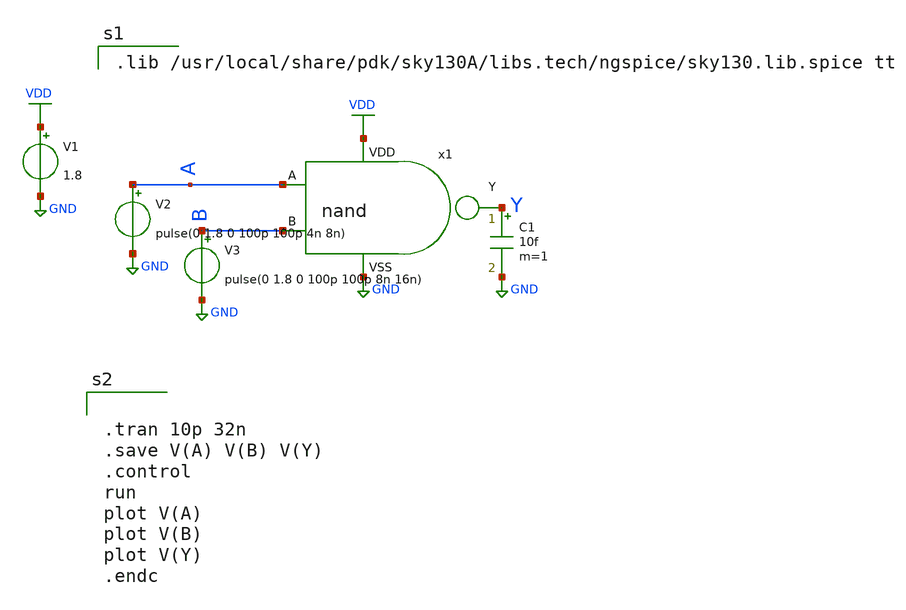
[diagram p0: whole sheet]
** sch_path: nand/design_circuit/tb_nand.sch
**.subckt tb_nand
x1 A B Y VDD GND nand
C1 Y GND 10f m=1
V1 VDD GND 1.8
V2 A GND pulse(0 1.8 0 100p 100p 4n 8n)
V3 B GND pulse(0 1.8 0 100p 100p 8n 16n)
**** begin user architecture code

.lib /usr/local/share/pdk/sky130A/libs.tech/ngspice/sky130.lib.spice tt



.tran 10p 32n
.save V(A) V(B) V(Y)
.control
run
plot V(A)
plot V(B)
plot V(Y)
.endc


**** end user architecture code
**.ends

* expanding   symbol:  nand.sym # of pins=5
** sym_path: nand/design_circuit/nand.sym
** sch_path: nand/design_circuit/nand.sch
.subckt nand A B Y VDD VSS
*.ipin A
*.ipin B
*.ipin VDD
*.ipin VSS
*.opin Y
XM1 Y A VDD VDD sky130_fd_pr__pfet_01v8 L=0.15 W=1 nf=1 ad='int((nf+1)/2) * W/nf * 0.29' as='int((nf+2)/2) * W/nf * 0.29'
+ pd='2*int((nf+1)/2) * (W/nf + 0.29)' ps='2*int((nf+2)/2) * (W/nf + 0.29)' nrd='0.29 / W' nrs='0.29 / W'
+ sa=0 sb=0 sd=0 mult=1 m=1
XM2 Y B VDD VDD sky130_fd_pr__pfet_01v8 L=0.15 W=1 nf=1 ad='int((nf+1)/2) * W/nf * 0.29' as='int((nf+2)/2) * W/nf * 0.29'
+ pd='2*int((nf+1)/2) * (W/nf + 0.29)' ps='2*int((nf+2)/2) * (W/nf + 0.29)' nrd='0.29 / W' nrs='0.29 / W'
+ sa=0 sb=0 sd=0 mult=1 m=1
XM3 Y B net1 VSS sky130_fd_pr__nfet_01v8 L=0.15 W=1 nf=1 ad='int((nf+1)/2) * W/nf * 0.29' as='int((nf+2)/2) * W/nf * 0.29'
+ pd='2*int((nf+1)/2) * (W/nf + 0.29)' ps='2*int((nf+2)/2) * (W/nf + 0.29)' nrd='0.29 / W' nrs='0.29 / W'
+ sa=0 sb=0 sd=0 mult=1 m=1
XM4 net1 A VSS VSS sky130_fd_pr__nfet_01v8 L=0.15 W=1 nf=1 ad='int((nf+1)/2) * W/nf * 0.29' as='int((nf+2)/2) * W/nf * 0.29'
+ pd='2*int((nf+1)/2) * (W/nf + 0.29)' ps='2*int((nf+2)/2) * (W/nf + 0.29)' nrd='0.29 / W' nrs='0.29 / W'
+ sa=0 sb=0 sd=0 mult=1 m=1
.ends

.GLOBAL VDD
.GLOBAL GND
.end
